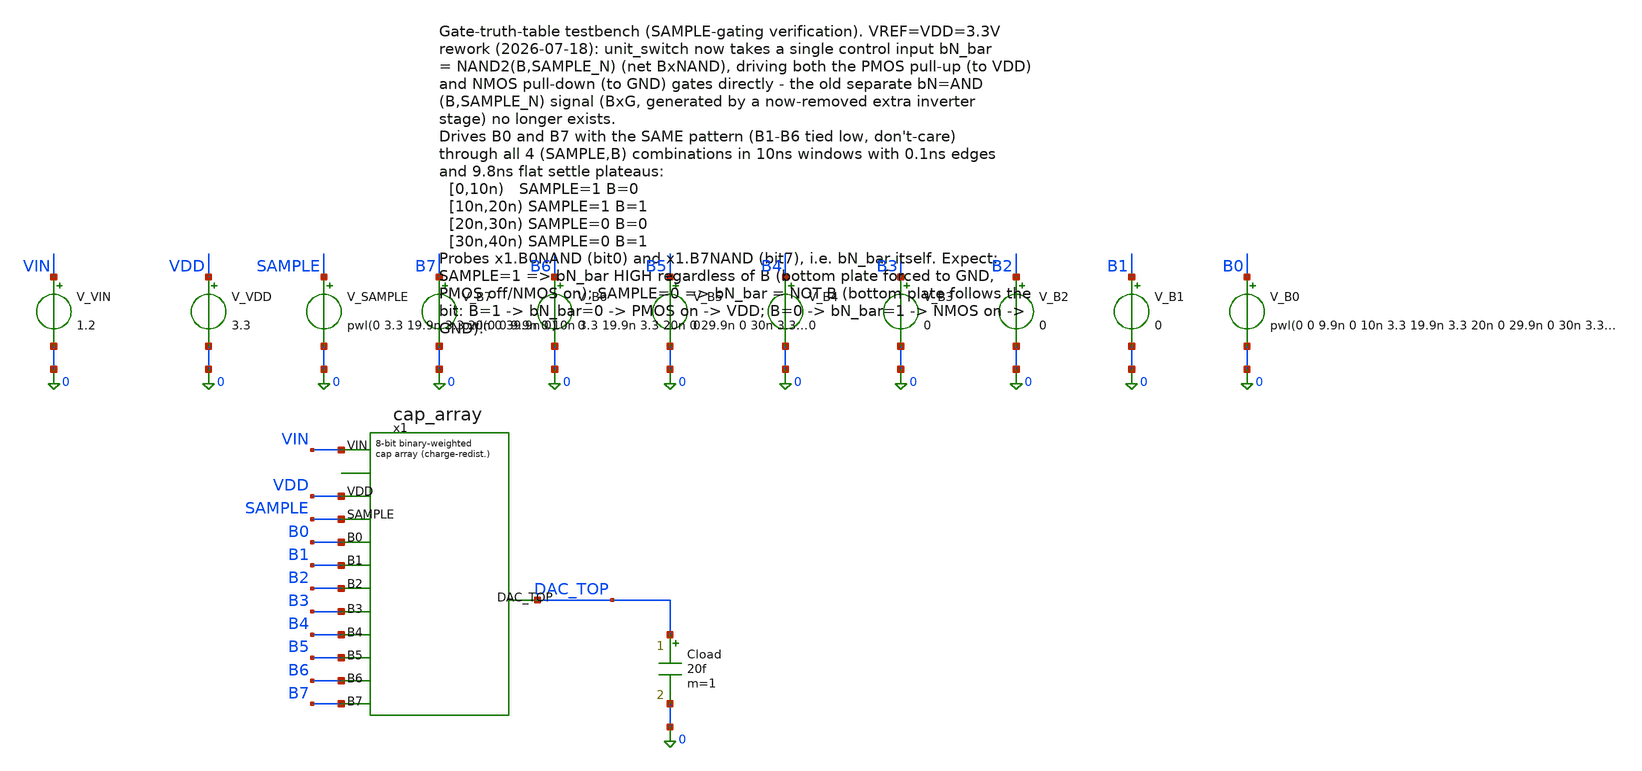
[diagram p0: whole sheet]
** sch_path: dac/sim/tb_gate_truth.sch
**.subckt tb_gate_truth
V_VIN VIN 0 1.2
V_VDD VDD 0 3.3
V_SAMPLE SAMPLE 0 pwl(0 3.3 19.9n 3.3 20n 0 39.9n 0)
V_B7 B7 0 pwl(0 0 9.9n 0 10n 3.3 19.9n 3.3 20n 0 29.9n 0 30n 3.3 39.9n 3.3)
V_B6 B6 0 0
V_B5 B5 0 0
V_B4 B4 0 0
V_B3 B3 0 0
V_B2 B2 0 0
V_B1 B1 0 0
V_B0 B0 0 pwl(0 0 9.9n 0 10n 3.3 19.9n 3.3 20n 0 29.9n 0 30n 3.3 39.9n 3.3)
Cload DAC_TOP 0 20f m=1
x1 VIN VDD SAMPLE B0 B1 B2 B3 B4 B5 B6 B7 DAC_TOP cap_array
**** begin user architecture code


.param nfet_wid=0.42u nfet_len=0.28u
.param mim_corner_1p0fF=1 mim_corner_1p5fF=1 mim_corner_2p0fF=1
.param mc_c_cox_1p0fF=0 mc_c_cox_1p5fF=0 mc_c_cox_2p0fF=0
.param var_vth=0 var_k=0
.lib /foss/pdks/gf180mcuD/libs.tech/ngspice/sm141064.ngspice typical
.lib /foss/pdks/gf180mcuD/libs.tech/ngspice/sm141064.ngspice cap_mim
.include /foss/pdks/gf180mcuD/libs.tech/ngspice/design.ngspice
.options savecurrents
.control
save all
tran 0.01n 40n
* bit0 truth table (bN_bar = x1.B0NAND)
meas tran b0nand_s1_b0 FIND v(x1.B0NAND) AT=5n
meas tran b0nand_s1_b1 FIND v(x1.B0NAND) AT=15n
meas tran b0nand_s0_b0 FIND v(x1.B0NAND) AT=25n
meas tran b0nand_s0_b1 FIND v(x1.B0NAND) AT=35n
* bit7 truth table (bN_bar = x1.B7NAND)
meas tran b7nand_s1_b0 FIND v(x1.B7NAND) AT=5n
meas tran b7nand_s1_b1 FIND v(x1.B7NAND) AT=15n
meas tran b7nand_s0_b0 FIND v(x1.B7NAND) AT=25n
meas tran b7nand_s0_b1 FIND v(x1.B7NAND) AT=35n
echo bit0_bN_bar_truth_table_V_s1b0_s1b1_s0b0_s0b1:
print b0nand_s1_b0 b0nand_s1_b1 b0nand_s0_b0 b0nand_s0_b1
echo bit7_bN_bar_truth_table_V_s1b0_s1b1_s0b0_s0b1:
print b7nand_s1_b0 b7nand_s1_b1 b7nand_s0_b0 b7nand_s0_b1
* bottom-plate (VOUT) node sanity: bit0 net1, bit7 net8
meas tran vout0_s0_b1 FIND v(x1.net1) AT=35n
meas tran vout7_s0_b1 FIND v(x1.net8) AT=35n
meas tran vout0_s0_b0 FIND v(x1.net1) AT=25n
meas tran vout7_s0_b0 FIND v(x1.net8) AT=25n
echo bottom_plate_V_bit0_bit7_at_S0B1_expect_VDD:
print vout0_s0_b1 vout7_s0_b1
echo bottom_plate_V_bit0_bit7_at_S0B0_expect_GND:
print vout0_s0_b0 vout7_s0_b0
.endc


**** end user architecture code
**.ends
.end
